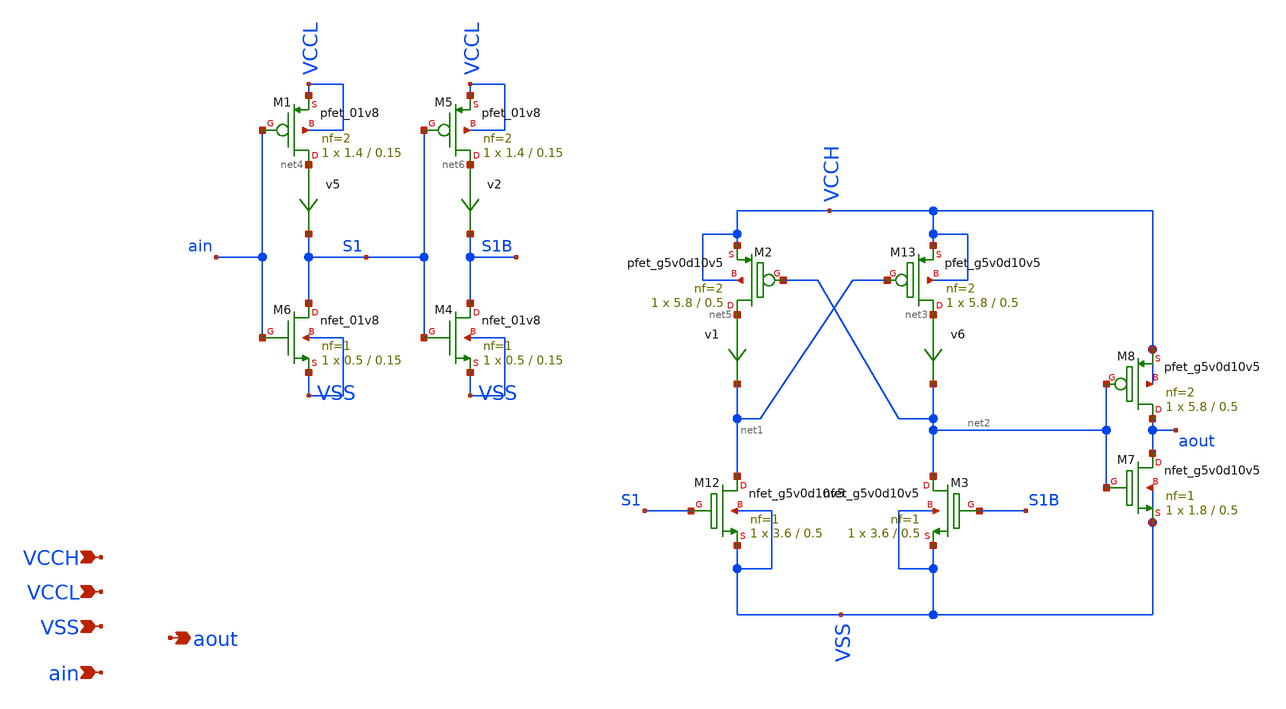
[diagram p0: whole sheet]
** sch_path: xschem/levelShifter2.sch
**.subckt levelShifter2 VCCL VSS ain aout VCCH
*.ipin VCCL
*.ipin VSS
*.ipin ain
*.opin aout
*.ipin VCCH
v6 net3 net2 0
.save i(v6)
XM12 net1 S1 VSS VSS sky130_fd_pr__nfet_g5v0d10v5 L=0.5 W=3.6 nf=1 ad='int((nf+1)/2) * W/nf * 0.29' as='int((nf+2)/2) * W/nf * 0.29'
+ pd='2*int((nf+1)/2) * (W/nf + 0.29)' ps='2*int((nf+2)/2) * (W/nf + 0.29)' nrd='0.29 / W' nrs='0.29 / W'
+ sa=0 sb=0 sd=0 mult=1 m=1
XM13 net3 net1 VCCH VCCH sky130_fd_pr__pfet_g5v0d10v5 L=0.5 W=5.8 nf=2 ad='int((nf+1)/2) * W/nf * 0.29'
+ as='int((nf+2)/2) * W/nf * 0.29' pd='2*int((nf+1)/2) * (W/nf + 0.29)' ps='2*int((nf+2)/2) * (W/nf + 0.29)'
+ nrd='0.29 / W' nrs='0.29 / W' sa=0 sb=0 sd=0 mult=1 m=1
v5 net4 S1 0
.save i(v5)
XM6 S1 ain VSS VSS sky130_fd_pr__nfet_01v8 L=0.15 W=0.5 nf=1 ad='int((nf+1)/2) * W/nf * 0.29' as='int((nf+2)/2) * W/nf * 0.29'
+ pd='2*int((nf+1)/2) * (W/nf + 0.29)' ps='2*int((nf+2)/2) * (W/nf + 0.29)' nrd='0.29 / W' nrs='0.29 / W'
+ sa=0 sb=0 sd=0 mult=1 m=1
XM1 net4 ain VCCL VCCL sky130_fd_pr__pfet_01v8 L=0.15 W=1.4 nf=2 ad='int((nf+1)/2) * W/nf * 0.29' as='int((nf+2)/2) * W/nf * 0.29'
+ pd='2*int((nf+1)/2) * (W/nf + 0.29)' ps='2*int((nf+2)/2) * (W/nf + 0.29)' nrd='0.29 / W' nrs='0.29 / W'
+ sa=0 sb=0 sd=0 mult=1 m=1
v1 net5 net1 0
.save i(v1)
XM2 net5 net2 VCCH VCCH sky130_fd_pr__pfet_g5v0d10v5 L=0.5 W=5.8 nf=2 ad='int((nf+1)/2) * W/nf * 0.29'
+ as='int((nf+2)/2) * W/nf * 0.29' pd='2*int((nf+1)/2) * (W/nf + 0.29)' ps='2*int((nf+2)/2) * (W/nf + 0.29)'
+ nrd='0.29 / W' nrs='0.29 / W' sa=0 sb=0 sd=0 mult=1 m=1
XM3 net2 S1B VSS VSS sky130_fd_pr__nfet_g5v0d10v5 L=0.5 W=3.6 nf=1 ad='int((nf+1)/2) * W/nf * 0.29' as='int((nf+2)/2) * W/nf * 0.29'
+ pd='2*int((nf+1)/2) * (W/nf + 0.29)' ps='2*int((nf+2)/2) * (W/nf + 0.29)' nrd='0.29 / W' nrs='0.29 / W'
+ sa=0 sb=0 sd=0 mult=1 m=1
v2 net6 S1B 0
.save i(v2)
XM4 S1B S1 VSS VSS sky130_fd_pr__nfet_01v8 L=0.15 W=0.5 nf=1 ad='int((nf+1)/2) * W/nf * 0.29' as='int((nf+2)/2) * W/nf * 0.29'
+ pd='2*int((nf+1)/2) * (W/nf + 0.29)' ps='2*int((nf+2)/2) * (W/nf + 0.29)' nrd='0.29 / W' nrs='0.29 / W'
+ sa=0 sb=0 sd=0 mult=1 m=1
XM5 net6 S1 VCCL VCCL sky130_fd_pr__pfet_01v8 L=0.15 W=1.4 nf=2 ad='int((nf+1)/2) * W/nf * 0.29' as='int((nf+2)/2) * W/nf * 0.29'
+ pd='2*int((nf+1)/2) * (W/nf + 0.29)' ps='2*int((nf+2)/2) * (W/nf + 0.29)' nrd='0.29 / W' nrs='0.29 / W'
+ sa=0 sb=0 sd=0 mult=1 m=1
XM7 aout net2 VSS VSS sky130_fd_pr__nfet_g5v0d10v5 L=0.5 W=1.8 nf=1 ad='int((nf+1)/2) * W/nf * 0.29'
+ as='int((nf+2)/2) * W/nf * 0.29' pd='2*int((nf+1)/2) * (W/nf + 0.29)' ps='2*int((nf+2)/2) * (W/nf + 0.29)'
+ nrd='0.29 / W' nrs='0.29 / W' sa=0 sb=0 sd=0 mult=1 m=1
XM8 aout net2 VCCH VCCH sky130_fd_pr__pfet_g5v0d10v5 L=0.5 W=5.8 nf=2 ad='int((nf+1)/2) * W/nf * 0.29'
+ as='int((nf+2)/2) * W/nf * 0.29' pd='2*int((nf+1)/2) * (W/nf + 0.29)' ps='2*int((nf+2)/2) * (W/nf + 0.29)'
+ nrd='0.29 / W' nrs='0.29 / W' sa=0 sb=0 sd=0 mult=1 m=1
**.ends
.end
